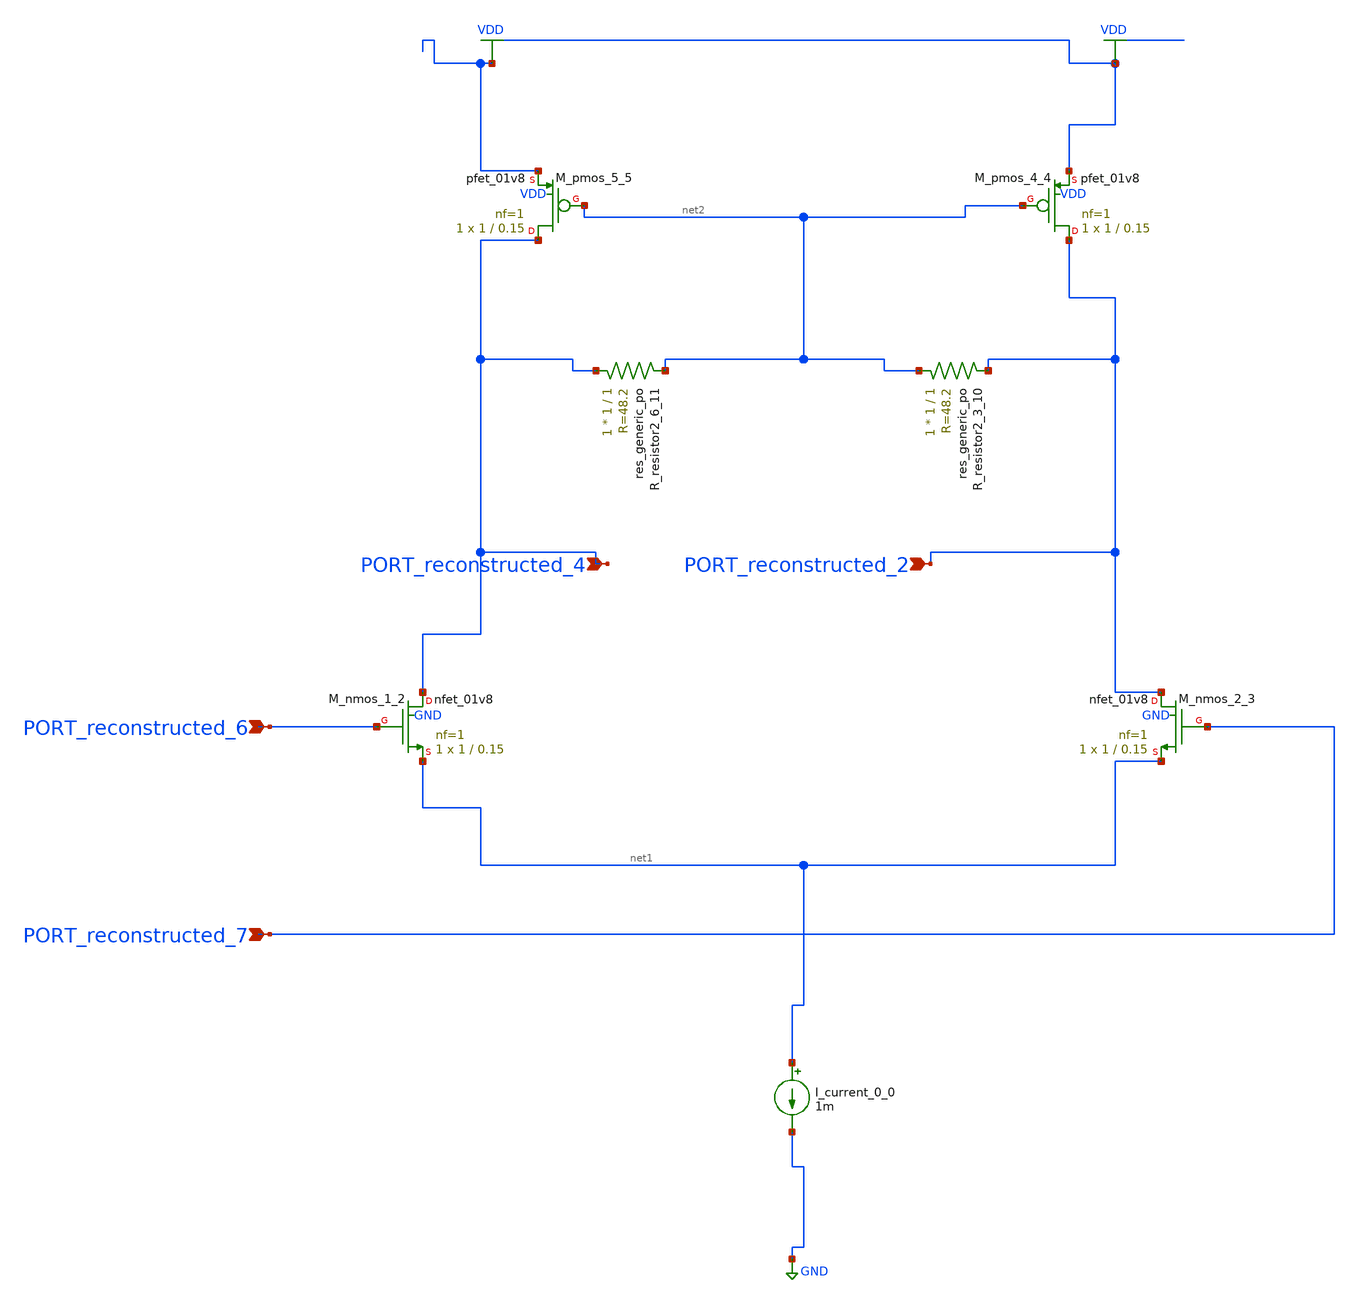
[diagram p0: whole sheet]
** sch_path: schematics/AMSNet/222.sch
**.subckt 222 PORT_reconstructed_6 PORT_reconstructed_7 PORT_reconstructed_2 PORT_reconstructed_4
*.ipin PORT_reconstructed_6
*.ipin PORT_reconstructed_7
*.ipin PORT_reconstructed_2
*.ipin PORT_reconstructed_4
I_current_0_0 net1 GND 1m
XM_nmos_1_2 PORT_reconstructed_4 PORT_reconstructed_6 net1 GND sky130_fd_pr__nfet_01v8 L=0.15 W=1 nf=1
+ ad='int((1 + 1)/2) * 1 / 1 * 0.29' as='int((1 + 2)/2) * 1 / 1 * 0.29' pd='2*int((1 + 1)/2) * (1 / 1 + 0.29)'
+ ps='2*int((1 + 2)/2) * (1 / 1 + 0.29)' nrd='0.29 / 1 ' nrs='0.29 / 1 ' sa=0 sb=0 sd=0 mult=1 m=1
XM_nmos_2_3 PORT_reconstructed_2 PORT_reconstructed_7 net1 GND sky130_fd_pr__nfet_01v8 L=0.15 W=1 nf=1
+ ad='int((1 + 1)/2) * 1 / 1 * 0.29' as='int((1 + 2)/2) * 1 / 1 * 0.29' pd='2*int((1 + 1)/2) * (1 / 1 + 0.29)'
+ ps='2*int((1 + 2)/2) * (1 / 1 + 0.29)' nrd='0.29 / 1 ' nrs='0.29 / 1 ' sa=0 sb=0 sd=0 mult=1 m=1
XM_pmos_4_4 PORT_reconstructed_2 net2 VDD VDD sky130_fd_pr__pfet_01v8 L=0.15 W=1 nf=1 ad='int((1 + 1)/2) * 1 / 1 * 0.29'
+ as='int((1 + 2)/2) * 1 / 1 * 0.29' pd='2*int((1 + 1)/2) * (1 / 1 + 0.29)' ps='2*int((1 + 2)/2) * (1 / 1 + 0.29)'
+ nrd='0.29 / 1 ' nrs='0.29 / 1 ' sa=0 sb=0 sd=0 mult=1 m=1
XM_pmos_5_5 PORT_reconstructed_4 net2 VDD VDD sky130_fd_pr__pfet_01v8 L=0.15 W=1 nf=1 ad='int((1 + 1)/2) * 1 / 1 * 0.29'
+ as='int((1 + 2)/2) * 1 / 1 * 0.29' pd='2*int((1 + 1)/2) * (1 / 1 + 0.29)' ps='2*int((1 + 2)/2) * (1 / 1 + 0.29)'
+ nrd='0.29 / 1 ' nrs='0.29 / 1 ' sa=0 sb=0 sd=0 mult=1 m=1
XR_resistor2_3_10 net2 PORT_reconstructed_2 sky130_fd_pr__res_generic_po W=1 L=1 m=1
XR_resistor2_6_11 PORT_reconstructed_4 net2 sky130_fd_pr__res_generic_po W=1 L=1 m=1
**.ends
.GLOBAL GND
.GLOBAL VDD
.end
